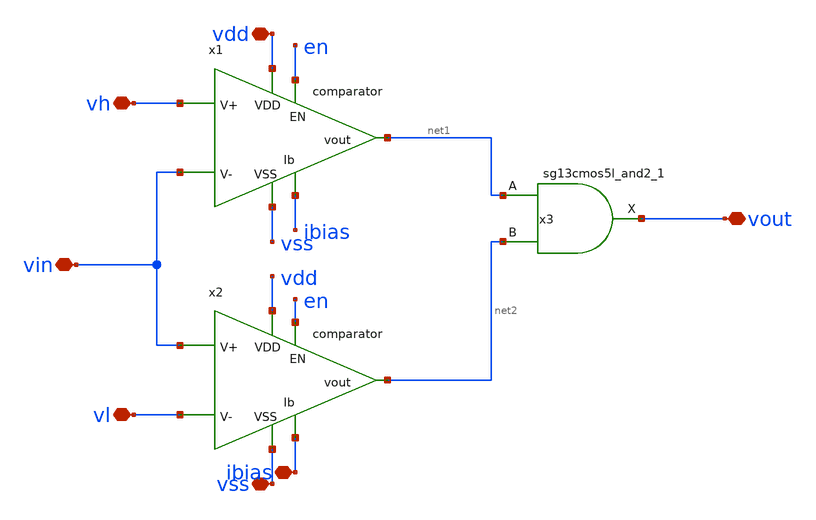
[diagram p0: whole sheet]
** sch_path: schematic/xschem/wind_comp/wind_comp.sch
**.subckt wind_comp vdd vout vl vh ibias vss vin
*.iopin vdd
*.iopin vout
*.iopin vl
*.iopin vh
*.iopin ibias
*.iopin vss
*.iopin vin
x1 vdd net1 vh vin ibias vss en comparator
x2 vdd net2 vin vl ibias vss en comparator
x3 vout net1 net2 VDD VSS sg13g2_and2_1
**.ends
.end
